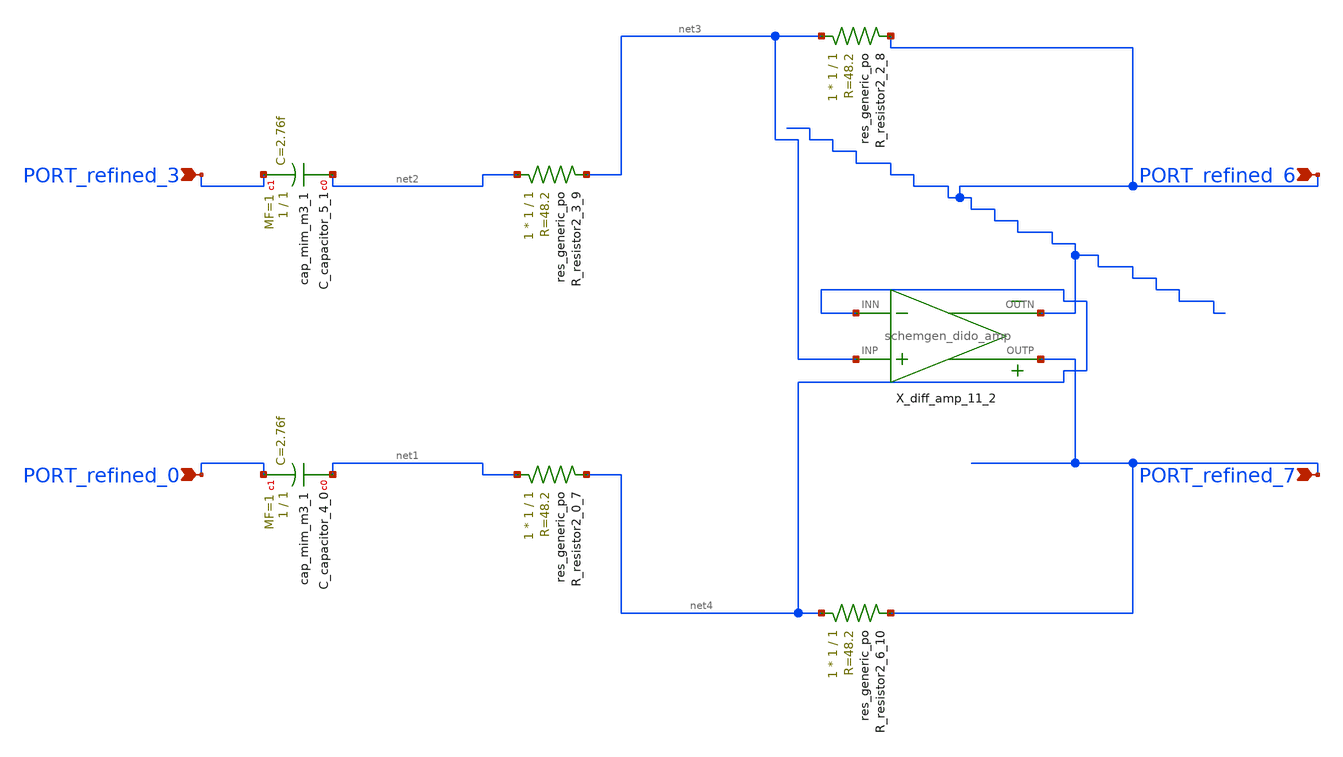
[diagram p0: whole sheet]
** sch_path: schematics/AMSNet/751.sch
**.subckt 751 PORT_refined_0 PORT_refined_6 PORT_refined_3 PORT_refined_7
*.ipin PORT_refined_0
*.ipin PORT_refined_6
*.ipin PORT_refined_3
*.ipin PORT_refined_7
XC_capacitor_4_0 net1 PORT_refined_0 sky130_fd_pr__cap_mim_m3_1 W=1 L=1 MF=1 m=1
XC_capacitor_5_1 net2 PORT_refined_3 sky130_fd_pr__cap_mim_m3_1 W=1 L=1 MF=1 m=1
X_diff_amp_11_2 net3 net4 PORT_refined_7 PORT_refined_6 schemgen_dido_amp
XR_resistor2_0_7 net1 net4 sky130_fd_pr__res_generic_po W=1 L=1 m=1
XR_resistor2_2_8 net3 PORT_refined_6 sky130_fd_pr__res_generic_po W=1 L=1 m=1
XR_resistor2_3_9 net2 net3 sky130_fd_pr__res_generic_po W=1 L=1 m=1
XR_resistor2_6_10 net4 PORT_refined_7 sky130_fd_pr__res_generic_po W=1 L=1 m=1
**.ends

* expanding   symbol:  schemgen_dido_amp.sym # of pins=4
** sym_path: symbols/schemgen_dido_amp.sym
.subckt schemgen_dido_amp INP INN OUTP OUTN
* SchemGen ideal fully differential op-amp: V(OUTP) - V(OUTN) = 1e5 * (V(INP) - V(INN))
EP OUTP 0 INP INN 5e4
EN OUTN 0 INN INP 5e4
.ends schemgen_dido_amp
.end
